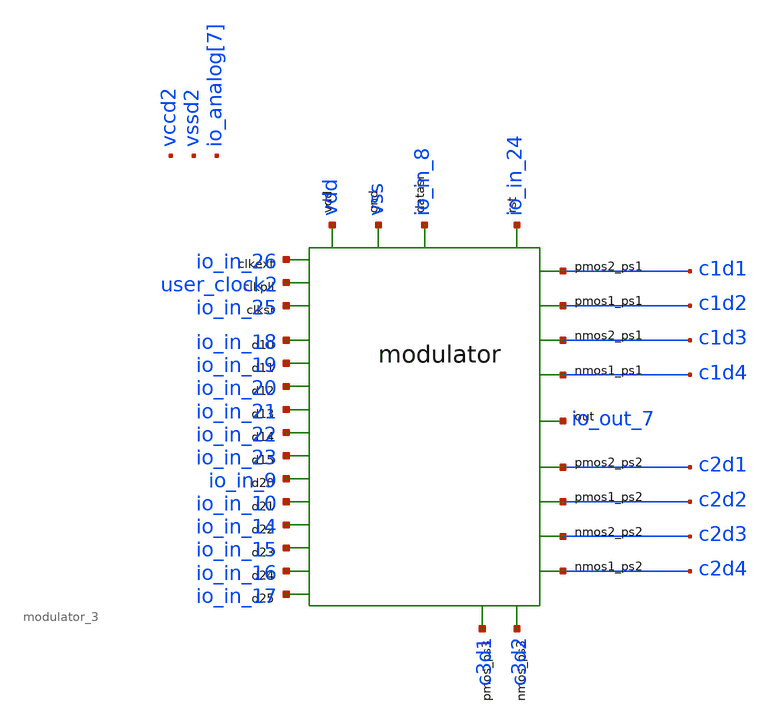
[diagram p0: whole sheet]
** sch_path: tb_modulator_time_3.sch
**.subckt tb_modulator_time_3
XMOD1 io_in_26 user_clock2 io_in_25 io_in_8 c1d4 c2d4 c1d3 c2d3 c3d2 c1d2 c2d2 c1d1 c2d1 c3d1
+ io_in_24 io_out_7 vss vdd io_in_18 io_in_19 io_in_20 io_in_21 io_in_22 io_in_23 io_in_9 io_in_10 io_in_14
+ io_in_15 io_in_16 io_in_17 Modulator
**** begin user architecture code


.lib /foss/pdks/sky130A/libs.tech/ngspice/sky130.lib.spice TT
.include /foss/designs/AC3E_Open3LFCC_V2_repo/xschem/Modulator_3.spice
*.include /foss/pdks/sky130A/libs.ref/sky130_fd_sc_hd/spice/sky130_fd_sc_hd.spice





* Power supplies
Vdd vdd 0 DC 1.8
Vss vss 0 DC 0

*T es 78n*

* Reloj clk_pll
Vpll user_clock2 vss PULSE (0 1.8 0 100p 100p 39n 78n)

* Reloj clk_ext (este deberia ser el que le demos con una fpga)
Vclk io_in_26 vss PULSE (0 1.8 0 100p 100p 39n 78n)

* Reset parte en 2*T y dura 3*T
Vreset io_in_24 vss PULSE (0 1.8 156n 100p 100p 234n 1e3)

*CLK_SR PARTEN EN 8T Y DURAN 3T, Y EL PERIODO DURA 5T
*Vclk_sr io_in_25 vss PULSE (0 1.8 1950n 100p 100p 390n 1169n)
Vclk_sr01 io_in_25 clk_sr01 PULSE (0 1.8 624n 100p 100p 234n 1e3)
Vclk_sr02 clk_sr01 clk_sr02 PULSE (0 1.8 1014n 100p 100p 234n 1e3)
Vclk_sr03 clk_sr02 clk_sr03 PULSE (0 1.8 1404n 100p 100p 234n 1e3)
Vclk_sr04 clk_sr03 clk_sr04 PULSE (0 1.8 1794n 100p 100p 234n 1e3)
Vclk_sr05 clk_sr04 clk_sr05 PULSE (0 1.8 2184n 100p 100p 234n 1e3)
Vclk_sr06 clk_sr05 clk_sr06 PULSE (0 1.8 2574n 100p 100p 234n 1e3)
Vclk_sr07 clk_sr06 clk_sr07 PULSE (0 1.8 2964n 100p 100p 234n 1e3)
Vclk_sr08 clk_sr07 clk_sr08 PULSE (0 1.8 3354n 100p 100p 234n 1e3)
Vclk_sr09 clk_sr08 clk_sr09 PULSE (0 1.8 3744n 100p 100p 234n 1e3)
Vclk_sr10 clk_sr09 clk_sr10 PULSE (0 1.8 4134n 100p 100p 234n 1e3)
Vclk_sr11 clk_sr10 clk_sr11 PULSE (0 1.8 4524n 100p 100p 234n 1e3)
Vclk_sr12 clk_sr11 clk_sr12 PULSE (0 1.8 4914n 100p 100p 234n 1e3)
Vclk_sr13 clk_sr12 clk_sr13 PULSE (0 1.8 5304n 100p 100p 234n 1e3)
Vclk_sr14 clk_sr13 clk_sr14 PULSE (0 1.8 5694n 100p 100p 234n 1e3)
Vclk_sr15 clk_sr14 clk_sr15 PULSE (0 1.8 6084n 100p 100p 234n 1e3)
Vclk_sr16 clk_sr15 clk_sr16 PULSE (0 1.8 6474n 100p 100p 234n 1e3)
Vclk_sr17 clk_sr16 clk_sr17 PULSE (0 1.8 6864n 100p 100p 234n 1e3)
Vclk_sr18 clk_sr17 vss PULSE (0 1.8 7254n 100p 100p 234n 1e3)

* SI EL VALOR ES CERO(0) COMENTAR LINEA *

* Carga Shift register
*                     PULSE (de_voltaje a_voltaje parte_en 100p 100p dura 1e3)
* Data_SR (dt[0]) (1) parte en 7*T y dura 5*T
Vdata_sr01 io_in_8 sr01 PULSE (0 1.8 546n 100p 100p 390n 1e3)

* Data_SR (dt[1]) (1) parte en 12*T y dura 5*T
Vdata_sr02 sr01 sr02 PULSE (0 1.8 936n 100p 100p 390n 1e3)

* Data_SR (dt[2]) (0) parte en 17*T y dura 5*T
*Vdata_sr03 sr02 sr03 PULSE (0 1.8 1326n 100p 100p 390n 1e3)

* Data_SR (dt[3]) (0) parte en 22*P y dura 5*T
*Vdata_sr04 sr03 sr04 PULSE (0 1.8 1716n 100p 100p 390n 1e3)

* Data_SR (dt[4]) (0) parte en 27*T y dura 5*T
*Vdata_sr05 sr04 sr05 PULSE (0 1.8 2106n 100p 100p 390n 1e3)

* Data_SR (SELECTOR_SIGNAL_GENERATOR_1[0]) (0) parte en (7+5*5)T y dura 5*T
*Vdata_sr06 sr05 sr06 PULSE (0 1.8 2496n 100p 100p 390n 1e3)

* Data_SR (SELECTOR_SIGNAL_GENERATOR_1[1]) (0) parte (7+5*6)T y dura 5*T
*Vdata_sr07 sr06 sr07 PULSE (0 1.8 2886n 100p 100p 390n 1e3)

* Data_SR (SELECTOR_SIGNAL_GENERATOR_2[0]) (0) parte (7+5*7)T y dura 5*T
*Vdata_sr08 sr07 sr08 PULSE (0 1.8 3276n 100p 100p 390n 1e3)

* Data_SR (SELECTOR_SIGNAL_GENERATOR_2[2]) (1) parte (7+5*8)T y dura 5*T
Vdata_sr09 sr02 sr09 PULSE (0 1.8 3666n 100p 100p 390n 1e3)

* Data_SR (OUTPUT_SELECTOR_EXTERNAL[0]) (0) parte (7+5*9)T y dura 5*T
*Vdata_sr10 sr09 sr10 PULSE (0 1.8 4056n 100p 100p 390n 1e3)

* Data_SR (OUTPUT_SELECTOR_EXTERNAL[1]) (0) parte (7+5*10)T y dura 5*T
*Vdata_sr11 sr10 sr11 PULSE (0 1.8 4446n 100p 100p 390n 1e3)

* Data_SR (OUTPUT_SELECTOR_EXTERNAL[2]) (0) parte (7+5*11)T y dura 5*T
*Vdata_sr12 sr11 sr12 PULSE (0 1.8 4806n 100p 100p 390n 1e3)

* Data_SR (OUTPUT_SELECTOR_EXTERNAL[3]) (0) parte (7+5*12)T y dura 5*T
*Vdata_sr13 sr12 sr13 PULSE (0 1.8 5226n 100p 100p 390n 1e3)

* Data_SR (INPUT_SELECTOR) (0) parte (7+5*13)T y dura 5*T     **EN (1) PASAN LAS ENTRADAS DIRECTO A
*+ LAS SALIDAS**
*Vdata_sr14 sr09 sr14 PULSE (0 1.8 5616n 100p 100p 390n 1e3)

* Data_SR (CLK_SELECTOR) (0) parte en parte (7+5*14)T y dura 5*T    ** EN (1) USA EL CLK EXTERNO, EN
*+ (0) USA EL CLK DEL PLL**
*Vdata_sr15 sr14 sr15 PULSE (0 1.8 6006n 100p 100p 390n 1e3)

* Data_SR (PS_SELECTOR) (1) parte (7+5*15)T y dura 5*T   ** EN (1) LA SALIDA VA A PS1, EN (0) VA A
*+ PS2**
Vdata_sr16 sr09 sr16 PULSE (0 1.8 6396n 100p 100p 390n 1e3)

* Data_SR (PS3_SELECTOR) (0) parte (7+5*16)T y dura 5*T   ** EN (1) DEJA PASAR LAS SENALES d15 y d14
*+ DIRECTAMENTE A PS3 Y APAGA LAS SALIDAS A PS1 Y PS2, EN (0) FUNCIONA LA LOGICA DE PS_SELECTOR **
*Vdata_sr17 sr16 sr17 vss PULSE (0 1.8 6786n 100p 100p 390n 1e3)

*Data_SR (ENABLE_OUTPUT) (1) parte (7+5*17)T y dura 5*T  ** EN (1) DEJA PASAR LA SALIDA CONFIGURADA,
*+ EN (0) LAS SALIDAS PROVOCAN QUE LOS TRANSISTORES ESTEN ABIERTOS**
Vdata_sr18 sr16 vss PULSE (0 1.8 7176n 100p 100p 390n 1e3)

*Valores de entrada
Vd15 io_in_23 0 DC 0
Vd14 io_in_22 0 DC 1.8
Vd13 io_in_21 0 DC 1.8
Vd12 io_in_20 0 DC 1.8
Vd11 io_in_19 0 DC 0
Vd10 io_in_18 0 DC 0

* Vd15 io_in_23 es NMOS_PS3
* Vd14 io_in_22 es PMOS_PS3
* Vd13 io_in_21 es PMOS1_EXT
* Vd12 io_in_20 es NMOS1_EXT
* Vd11 io_in_19 es PMOS2_EXT
* Vd10 io_in_18 es NMOS2_EXT

Vd25 io_in_17 0 DC 1.8
Vd24 io_in_16 0 DC 0
Vd23 io_in_15 0 DC 1.8
Vd22 io_in_14 0 DC 1.8
Vd21 io_in_10 0 DC 1.8
Vd20 io_in_9 0 DC 0

.option scale=1e-6
.control
save all
tran 39n 10u
plot V(io_in_8) V(io_in_25) V(io_in_24)
plot V(c1d1)
plot V(c1d2)
plot V(c1d3)
plot V(c1d4)
plot V(c2d1) V(c2d2) V(c2d3) V(c2d4)
plot V(c3d1) V(c3d2)
.endc


**** end user architecture code
**.ends
.end
